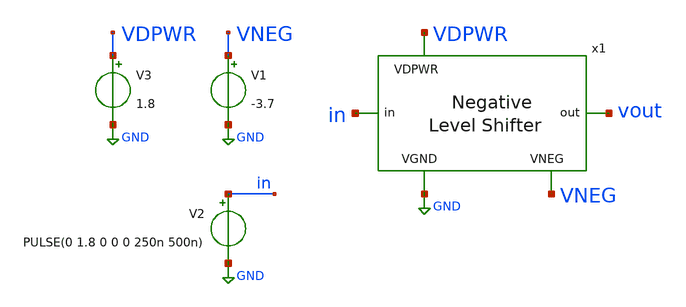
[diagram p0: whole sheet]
** sch_path: xschem/level_shifter_neg_tb.sch
**.subckt level_shifter_neg_tb
V1 VNEG GND -3.7
V2 in GND PULSE(0 1.8 0 0 0 250n 500n)
V3 VDPWR GND 1.8
x1 VDPWR in vout VNEG GND level_shifter_neg
**** begin user architecture code

** opencircuitdesign pdks install
.lib $::SKYWATER_MODELS/sky130.lib.spice tt





.tran 10n 10u
.save all

.control
run
write level_shifter_neg_tb.raw
.endc


**** end user architecture code
**.ends

* expanding   symbol:  level_shifter_neg.sym # of pins=5
** sym_path: xschem/level_shifter_neg.sym
** sch_path: xschem/level_shifter_neg.sch
.subckt level_shifter_neg VDPWR in out VNEG VGND
*.iopin VNEG
*.iopin VDPWR
*.ipin in
*.iopin VGND
*.opin out
XM6 in_b in VGND VGND sky130_fd_pr__nfet_01v8 L=3 W=1 nf=1 ad='int((nf+1)/2) * W/nf * 0.29' as='int((nf+2)/2) * W/nf * 0.29'
+ pd='2*int((nf+1)/2) * (W/nf + 0.29)' ps='2*int((nf+2)/2) * (W/nf + 0.29)' nrd='0.29 / W' nrs='0.29 / W'
+ sa=0 sb=0 sd=0 mult=1 m=1
XM5 in_b in VDPWR VDPWR sky130_fd_pr__pfet_01v8 L=3 W=1 nf=1 ad='int((nf+1)/2) * W/nf * 0.29' as='int((nf+2)/2) * W/nf * 0.29'
+ pd='2*int((nf+1)/2) * (W/nf + 0.29)' ps='2*int((nf+2)/2) * (W/nf + 0.29)' nrd='0.29 / W' nrs='0.29 / W'
+ sa=0 sb=0 sd=0 mult=1 m=1
XM1 mid_b in VDPWR VDPWR sky130_fd_pr__pfet_g5v0d10v5 L=1 W=3 nf=1 ad='int((nf+1)/2) * W/nf * 0.29' as='int((nf+2)/2) * W/nf * 0.29'
+ pd='2*int((nf+1)/2) * (W/nf + 0.29)' ps='2*int((nf+2)/2) * (W/nf + 0.29)' nrd='0.29 / W' nrs='0.29 / W'
+ sa=0 sb=0 sd=0 mult=1 m=1
XM2 mid in_b VDPWR VDPWR sky130_fd_pr__pfet_g5v0d10v5 L=1 W=3 nf=1 ad='int((nf+1)/2) * W/nf * 0.29' as='int((nf+2)/2) * W/nf * 0.29'
+ pd='2*int((nf+1)/2) * (W/nf + 0.29)' ps='2*int((nf+2)/2) * (W/nf + 0.29)' nrd='0.29 / W' nrs='0.29 / W'
+ sa=0 sb=0 sd=0 mult=1 m=1
XM4 mid mid_b VNEG VNEG sky130_fd_pr__nfet_g5v0d10v5 L=10 W=1 nf=1 ad='int((nf+1)/2) * W/nf * 0.29' as='int((nf+2)/2) * W/nf * 0.29'
+ pd='2*int((nf+1)/2) * (W/nf + 0.29)' ps='2*int((nf+2)/2) * (W/nf + 0.29)' nrd='0.29 / W' nrs='0.29 / W'
+ sa=0 sb=0 sd=0 mult=1 m=1
XM3 mid_b mid VNEG VNEG sky130_fd_pr__nfet_g5v0d10v5 L=10 W=1 nf=1 ad='int((nf+1)/2) * W/nf * 0.29' as='int((nf+2)/2) * W/nf * 0.29'
+ pd='2*int((nf+1)/2) * (W/nf + 0.29)' ps='2*int((nf+2)/2) * (W/nf + 0.29)' nrd='0.29 / W' nrs='0.29 / W'
+ sa=0 sb=0 sd=0 mult=1 m=1
XM7 out mid_b VGND VGND sky130_fd_pr__pfet_g5v0d10v5 L=3 W=2 nf=1 ad='int((nf+1)/2) * W/nf * 0.29' as='int((nf+2)/2) * W/nf * 0.29'
+ pd='2*int((nf+1)/2) * (W/nf + 0.29)' ps='2*int((nf+2)/2) * (W/nf + 0.29)' nrd='0.29 / W' nrs='0.29 / W'
+ sa=0 sb=0 sd=0 mult=1 m=1
XM8 out mid_b VNEG VNEG sky130_fd_pr__nfet_g5v0d10v5 L=3 W=1 nf=1 ad='int((nf+1)/2) * W/nf * 0.29' as='int((nf+2)/2) * W/nf * 0.29'
+ pd='2*int((nf+1)/2) * (W/nf + 0.29)' ps='2*int((nf+2)/2) * (W/nf + 0.29)' nrd='0.29 / W' nrs='0.29 / W'
+ sa=0 sb=0 sd=0 mult=1 m=1
.ends

.GLOBAL GND
.end
